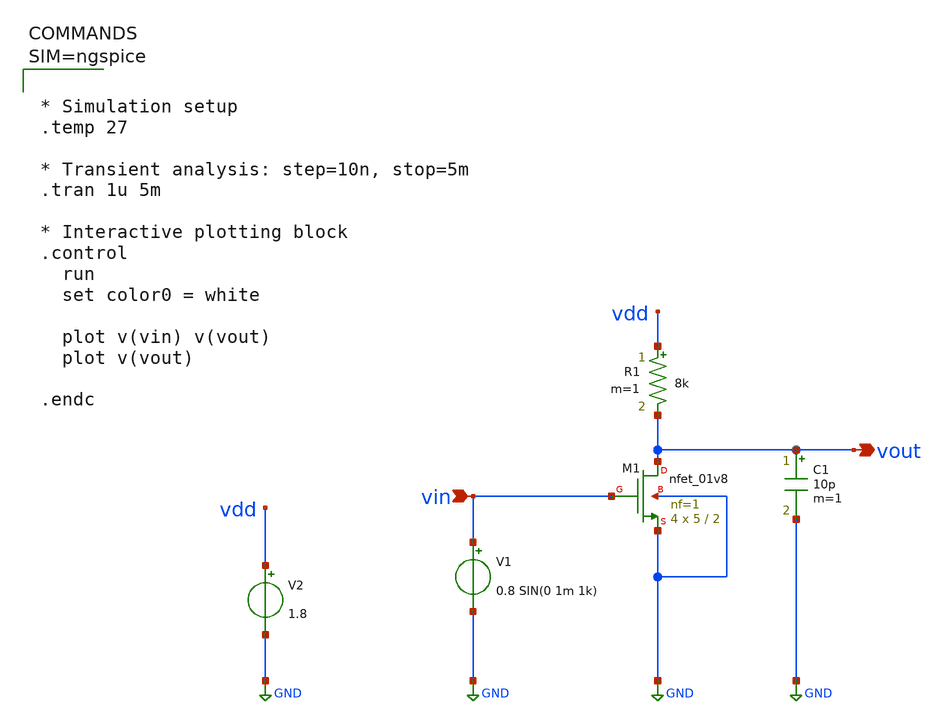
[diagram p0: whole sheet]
** sch_path: sch/NMOS_Restitive_Load_amp.sch
**.subckt NMOS_Restitive_Load_amp vout vin
*.opin vout
*.ipin vin
XM1 vout vin GND GND sky130_fd_pr__nfet_01v8 L=2 W=5 nf=1 ad='int((1 + 1)/2) * 5 / 1 * 0.29' as='int((1 + 2)/2) * 5 / 1 * 0.29'
+ pd='2*int((1 + 1)/2) * (5 / 1 + 0.29)' ps='2*int((1 + 2)/2) * (5 / 1 + 0.29)' nrd='0.29 / 5 ' nrs='0.29 / 5 '
+ sa=0 sb=0 sd=0 mult=4 m=4
V1 vin GND 0.8 SIN(0 1m 1k)
C1 vout GND 10p m=1
V2 vdd GND 1.8
R1 vdd vout 8k m=1
**** begin user architecture code

** opencircuitdesign pdks install
.lib $::SKYWATER_MODELS/sky130.lib.spice tt




* Simulation setup
.temp 27

* Transient analysis: step=10n, stop=5m
.tran 1u 5m

* Interactive plotting block
.control
  run
  set color0 = white

  plot v(vin) v(vout)
  plot v(vout)

.endc




**** end user architecture code
**.ends
.GLOBAL GND
.end
